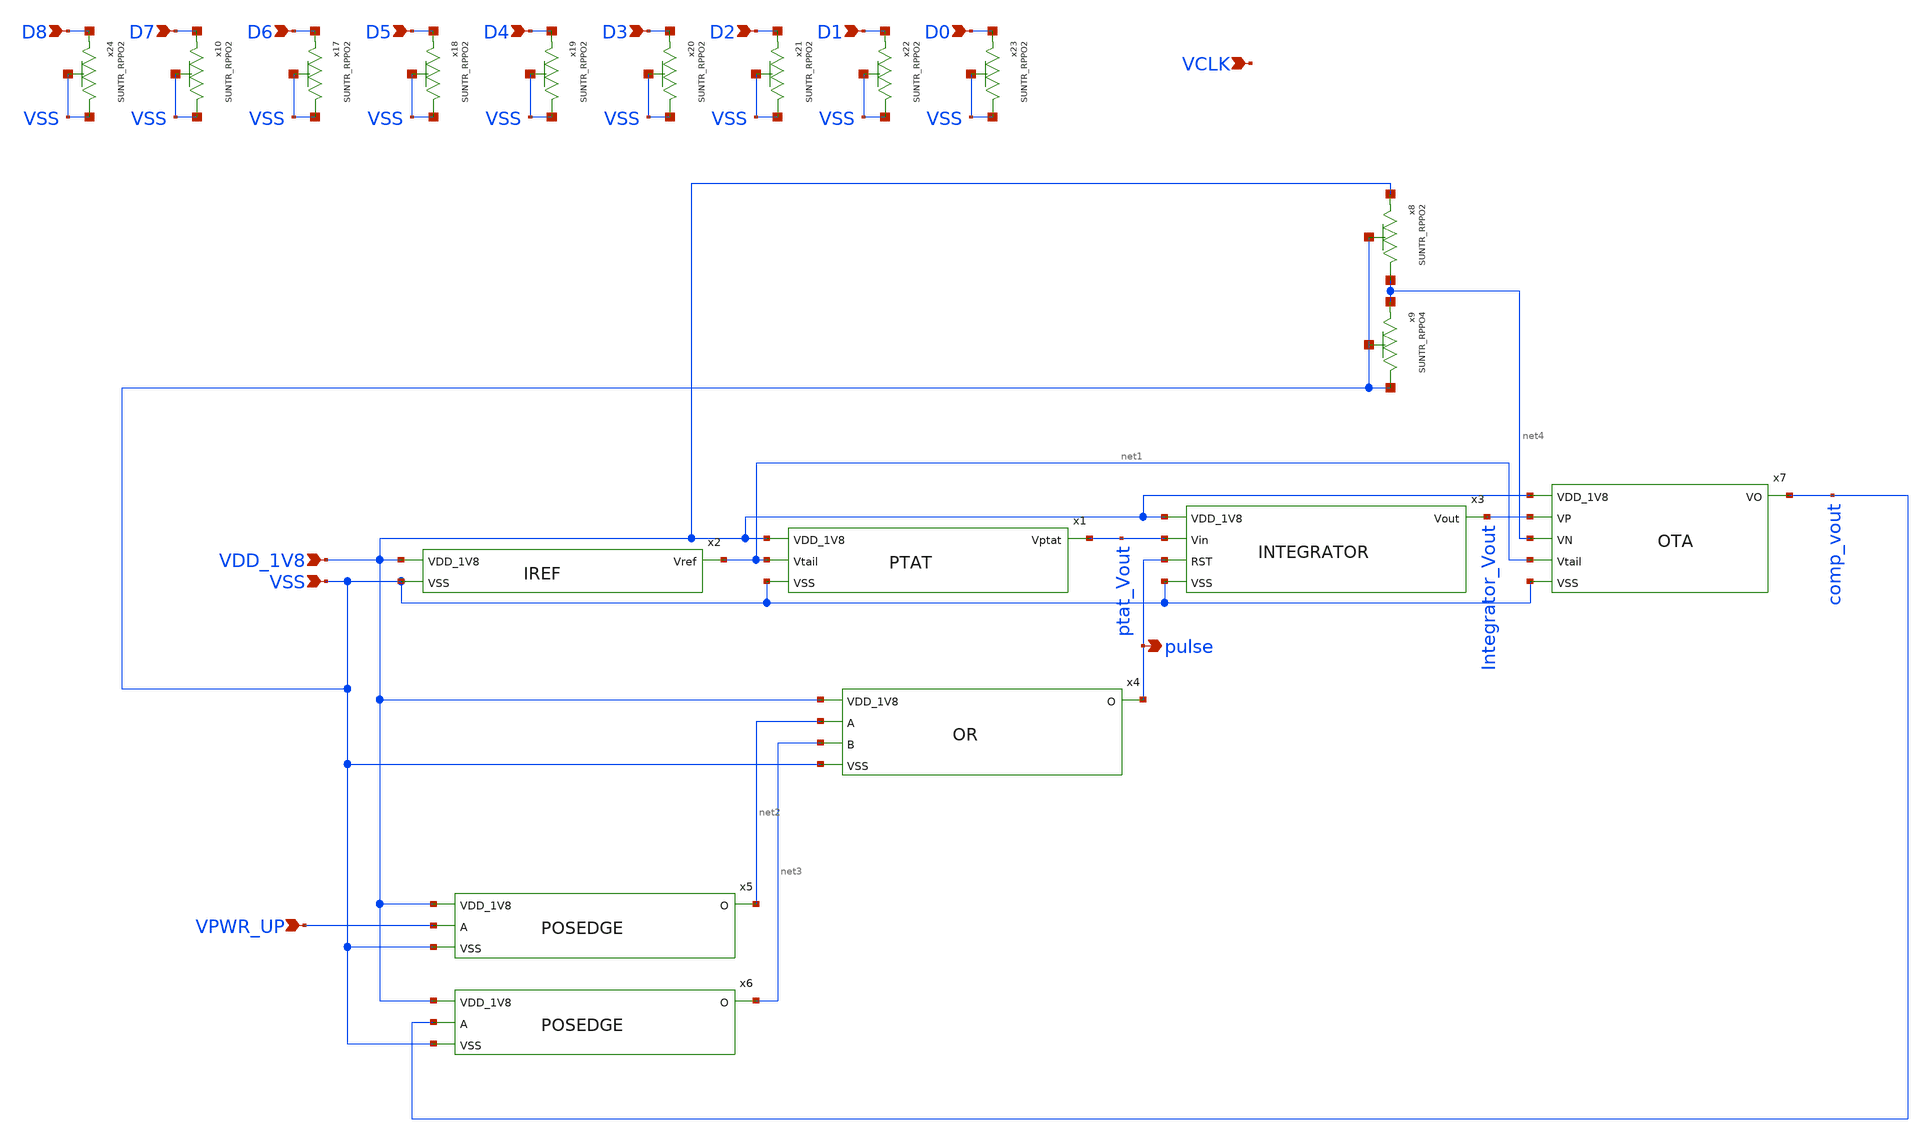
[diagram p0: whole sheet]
** sch_path: design/CNR_GR05_SKY130NM/final.sch
**.subckt final VDD_1V8 VSS VPWR_UP D7 D6 D5 D4 D3 D2 D1 D0 D8 VCLK pulse
*.ipin VDD_1V8
*.ipin VSS
*.ipin VPWR_UP
*.ipin D7
*.ipin D6
*.ipin D5
*.ipin D4
*.ipin D3
*.ipin D2
*.ipin D1
*.ipin D0
*.ipin D8
*.ipin VCLK
*.opin pulse
x1 VDD_1V8 net1 VSS ptat_Vout PTAT
x2 VDD_1V8 net1 VSS IREF
x3 VDD_1V8 ptat_Vout Integrator_Vout pulse VSS INTEGRATOR
x4 VDD_1V8 net2 net3 pulse VSS OR
x5 VDD_1V8 VPWR_UP net2 VSS POSEDGE
x6 VDD_1V8 comp_vout net3 VSS POSEDGE
x7 VDD_1V8 comp_vout Integrator_Vout net4 net1 VSS OTA
x8 net4 VDD_1V8 VSS SUNTR_RPPO2
x9 VSS net4 VSS SUNTR_RPPO4 xoffset=0 yoffset=0 angle=0
x10 VSS D7 VSS SUNTR_RPPO2
x17 VSS D6 VSS SUNTR_RPPO2
x18 VSS D5 VSS SUNTR_RPPO2
x19 VSS D4 VSS SUNTR_RPPO2
x20 VSS D3 VSS SUNTR_RPPO2
x21 VSS D2 VSS SUNTR_RPPO2
x22 VSS D1 VSS SUNTR_RPPO2
x23 VSS D0 VSS SUNTR_RPPO2
x24 VSS D8 VSS SUNTR_RPPO2
**.ends
.end
